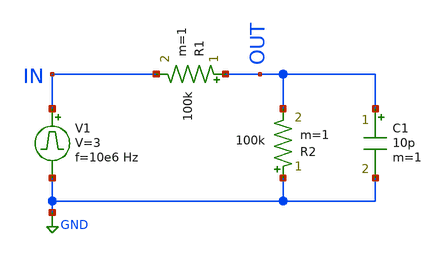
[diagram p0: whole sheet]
** sch_path: test_sch.sch
**.subckt test_sch
V1 IN GND pulse 0 3 '0.495/ 10e6 ' '0.01/10e6 ' '0.01/10e6 ' '0.49/10e6 ' '1/10e6 '
R1 OUT IN 100k m=1
R2 GND OUT 100k m=1
C1 OUT GND 10p m=1
**.ends
.GLOBAL GND
.end
